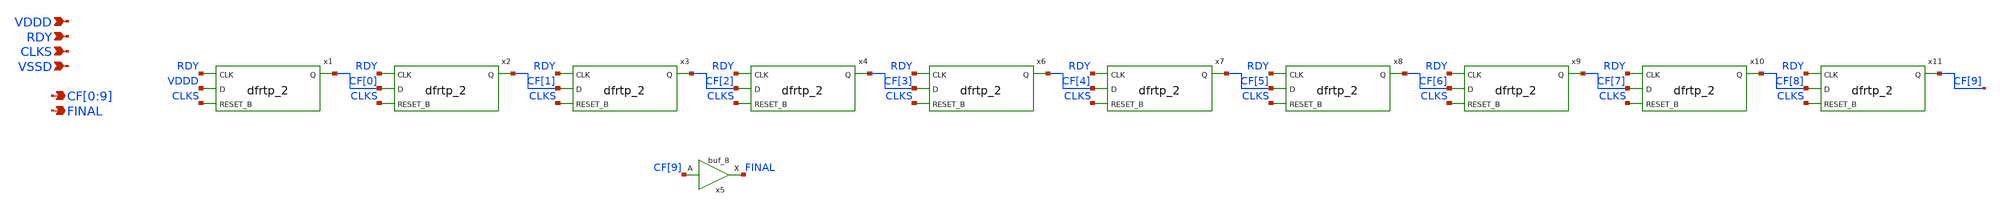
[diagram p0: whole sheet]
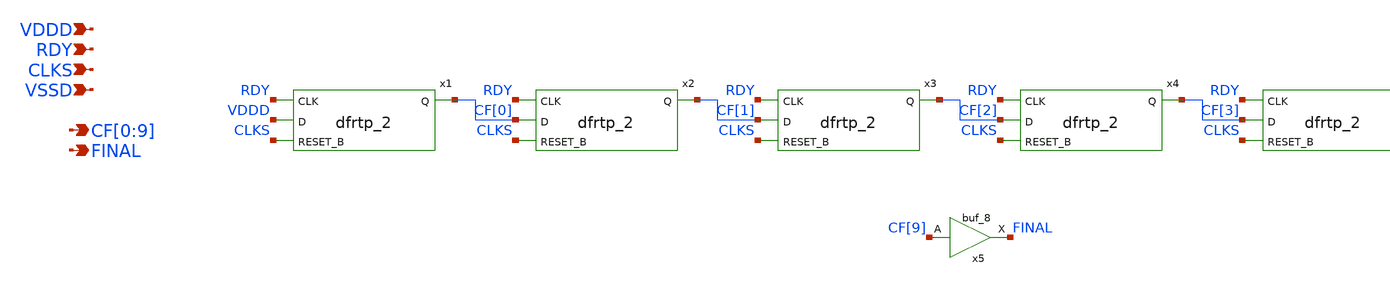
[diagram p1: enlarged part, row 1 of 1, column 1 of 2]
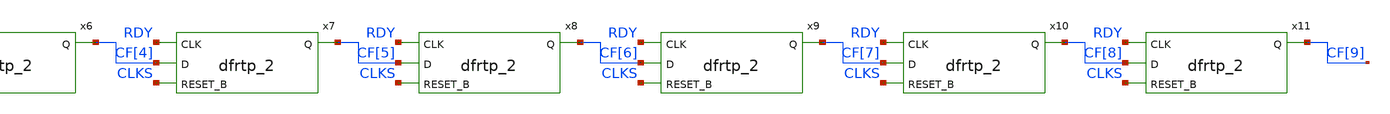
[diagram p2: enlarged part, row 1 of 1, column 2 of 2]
** sch_path: xschem/cyclic_flag.sch
**.subckt cyclic_flag RDY VDDD CLKS VSSD CF[0],CF[1],CF[2],CF[3],CF[4],CF[5],CF[6],CF[7],CF[8],CF[9]
*+ FINAL
*.ipin RDY
*.ipin VDDD
*.ipin CLKS
*.ipin VSSD
*.opin CF[0],CF[1],CF[2],CF[3],CF[4],CF[5],CF[6],CF[7],CF[8],CF[9]
*.opin FINAL
x1 RDY VDDD CLKS VSSD VSSD VDDD VDDD CF[0] sky130_fd_sc_hdll__dfrtp_2
x2 RDY CF[0] CLKS VSSD VSSD VDDD VDDD CF[1] sky130_fd_sc_hdll__dfrtp_2
x3 RDY CF[1] CLKS VSSD VSSD VDDD VDDD CF[2] sky130_fd_sc_hdll__dfrtp_2
x4 RDY CF[2] CLKS VSSD VSSD VDDD VDDD CF[3] sky130_fd_sc_hdll__dfrtp_2
x5 CF[9] VSSD VSSD VDDD VDDD FINAL sky130_fd_sc_hdll__buf_8
x6 RDY CF[3] CLKS VSSD VSSD VDDD VDDD CF[4] sky130_fd_sc_hdll__dfrtp_2
x7 RDY CF[4] CLKS VSSD VSSD VDDD VDDD CF[5] sky130_fd_sc_hdll__dfrtp_2
x8 RDY CF[5] CLKS VSSD VSSD VDDD VDDD CF[6] sky130_fd_sc_hdll__dfrtp_2
x9 RDY CF[6] CLKS VSSD VSSD VDDD VDDD CF[7] sky130_fd_sc_hdll__dfrtp_2
x10 RDY CF[7] CLKS VSSD VSSD VDDD VDDD CF[8] sky130_fd_sc_hdll__dfrtp_2
x11 RDY CF[8] CLKS VSSD VSSD VDDD VDDD CF[9] sky130_fd_sc_hdll__dfrtp_2
**.ends
.end
